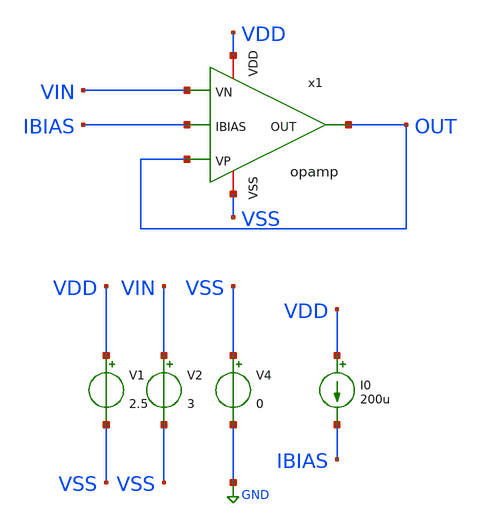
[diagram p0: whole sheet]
** sch_path: opamp_sementara/opamp/input-offset.sch
**.subckt input-offset
x1 VDD OUT VIN OUT IBIAS VSS opamp
I0 VDD IBIAS 200u
V1 VDD VSS 2.5
V2 VIN VSS 3
V4 VSS GND 0
**** begin user architecture code

** opencircuitdesign pdks install
.lib $::SKYWATER_MODELS/sky130.lib.spice mc





.control
  set noaskquit
  set wr_vecnames
  set wr_singlescale

  let mc_runs = 100
  let run = 0
  let vcm_target = 1.25

  * --- INIT VECTOR (100 entries) ---
  compose vos_vec values 0 0 0 0 0 0 0 0 0 0 0 0 0 0 0 0 0 0 0 0 0 0 0 0 0 0 0 0 0 0 0 0 0 0 0 0 0 0
+ 0 0 0 0 0 0 0 0 0 0 0 0 0 0 0 0 0 0 0 0 0 0 0 0 0 0 0 0 0 0 0 0 0 0 0 0 0 0 0 0 0 0 0 0 0 0 0 0 0 0 0
+ 0 0 0 0 0 0 0 0 0 0 0

  dowhile run < mc_runs
    reset

    * FIX ERROR SETSEED: Hitung dulu di variabel luar
    let current_seed = run + 1
    setseed $&current_seed

    * Jalankan DC Sweep (V1 adalah source yang di-sweep)
    dc V2 1.24 1.26 0.05m

    * Ekstraksi nilai Vin saat crossing
    meas dc vin_at_vcm when v(out)=vcm_target

    * Hitung Vos dalam uV dan masukkan ke vector
    let vos_val = (vcm_target - vin_at_vcm) * 1e6
    let vos_vec[run] = vos_val

    echo Iteration: $&run | Vos: $&vos_val uV
    let run = run + 1
  end

  * =============================================================
  * RE-FIXED CSV OUTPUT BLOCK (INDEX EVALUATION)
  * =============================================================
  shell rm -f vos_results.csv
  shell echo run,vos_uv > vos_results.csv

  let i = 0
  dowhile i < mc_runs
    let tmp_vos = vos_vec[i]
    echo $&i, $&tmp_vos >> vos_results.csv
    let i = i + 1
  end

  echo ==========================================================
  echo SELESAI! Cek 'vos_results.csv' di folder lo sekarang.
  print mean(vos_vec) std(vos_vec)
  echo ==========================================================
.endc



**** end user architecture code
**.ends

* expanding   symbol:  icdec-biomedical-pmic/opamp_sementara/opamp/opamp.sym # of pins=6
** sym_path: opamp_sementara/opamp/opamp.sym
** sch_path: opamp_sementara/opamp/opamp.sch
.subckt opamp VDD OUT VN VP IBIAS VSS
*.iopin VDD
*.ipin VP
*.ipin VN
*.ipin IBIAS
*.iopin VSS
*.opin OUT
XM1 net2 net1 VDD VDD sky130_fd_pr__pfet_g5v0d10v5 L=1.25 W=75.2 nf=1 ad='int((nf+1)/2) * W/nf * 0.29'
+ as='int((nf+2)/2) * W/nf * 0.29' pd='2*int((nf+1)/2) * (W/nf + 0.29)' ps='2*int((nf+2)/2) * (W/nf + 0.29)'
+ nrd='0.29 / W' nrs='0.29 / W' sa=0 sb=0 sd=0 mult=1 m=1
XM2 net1 net1 VDD VDD sky130_fd_pr__pfet_g5v0d10v5 L=1.25 W=75.2 nf=1 ad='int((nf+1)/2) * W/nf * 0.29'
+ as='int((nf+2)/2) * W/nf * 0.29' pd='2*int((nf+1)/2) * (W/nf + 0.29)' ps='2*int((nf+2)/2) * (W/nf + 0.29)'
+ nrd='0.29 / W' nrs='0.29 / W' sa=0 sb=0 sd=0 mult=1 m=1
XM5 net2 VN net3 VSS sky130_fd_pr__nfet_g5v0d10v5 L=0.5 W=38 nf=1 ad='int((nf+1)/2) * W/nf * 0.29' as='int((nf+2)/2) * W/nf * 0.29'
+ pd='2*int((nf+1)/2) * (W/nf + 0.29)' ps='2*int((nf+2)/2) * (W/nf + 0.29)' nrd='0.29 / W' nrs='0.29 / W'
+ sa=0 sb=0 sd=0 mult=1 m=1
XM6 net1 VP net3 VSS sky130_fd_pr__nfet_g5v0d10v5 L=0.5 W=38 nf=1 ad='int((nf+1)/2) * W/nf * 0.29' as='int((nf+2)/2) * W/nf * 0.29'
+ pd='2*int((nf+1)/2) * (W/nf + 0.29)' ps='2*int((nf+2)/2) * (W/nf + 0.29)' nrd='0.29 / W' nrs='0.29 / W'
+ sa=0 sb=0 sd=0 mult=1 m=1
XM23 net3 IBIAS VSS VSS sky130_fd_pr__nfet_g5v0d10v5 L=1.25 W=60 nf=1 ad='int((nf+1)/2) * W/nf * 0.29'
+ as='int((nf+2)/2) * W/nf * 0.29' pd='2*int((nf+1)/2) * (W/nf + 0.29)' ps='2*int((nf+2)/2) * (W/nf + 0.29)'
+ nrd='0.29 / W' nrs='0.29 / W' sa=0 sb=0 sd=0 mult=1 m=1
XM24 IBIAS IBIAS VSS VSS sky130_fd_pr__nfet_g5v0d10v5 L=1.25 W=60 nf=1 ad='int((nf+1)/2) * W/nf * 0.29'
+ as='int((nf+2)/2) * W/nf * 0.29' pd='2*int((nf+1)/2) * (W/nf + 0.29)' ps='2*int((nf+2)/2) * (W/nf + 0.29)'
+ nrd='0.29 / W' nrs='0.29 / W' sa=0 sb=0 sd=0 mult=1 m=1
XM27 OUT net2 VDD VDD sky130_fd_pr__pfet_g5v0d10v5 L=1.25 W=160 nf=1 ad='int((nf+1)/2) * W/nf * 0.29'
+ as='int((nf+2)/2) * W/nf * 0.29' pd='2*int((nf+1)/2) * (W/nf + 0.29)' ps='2*int((nf+2)/2) * (W/nf + 0.29)'
+ nrd='0.29 / W' nrs='0.29 / W' sa=0 sb=0 sd=0 mult=1 m=1
XM28 OUT IBIAS VSS VSS sky130_fd_pr__nfet_g5v0d10v5 L=1.25 W=60 nf=1 ad='int((nf+1)/2) * W/nf * 0.29'
+ as='int((nf+2)/2) * W/nf * 0.29' pd='2*int((nf+1)/2) * (W/nf + 0.29)' ps='2*int((nf+2)/2) * (W/nf + 0.29)'
+ nrd='0.29 / W' nrs='0.29 / W' sa=0 sb=0 sd=0 mult=1 m=1
XC1 net4 net2 sky130_fd_pr__cap_mim_m3_1 W=25 L=25 MF=8 m=8
XM29 OUT VSS net4 VDD sky130_fd_pr__pfet_g5v0d10v5 L=0.9 W=20 nf=1 ad='int((nf+1)/2) * W/nf * 0.29' as='int((nf+2)/2) * W/nf * 0.29'
+ pd='2*int((nf+1)/2) * (W/nf + 0.29)' ps='2*int((nf+2)/2) * (W/nf + 0.29)' nrd='0.29 / W' nrs='0.29 / W'
+ sa=0 sb=0 sd=0 mult=1 m=1
.ends

.GLOBAL GND
.end
